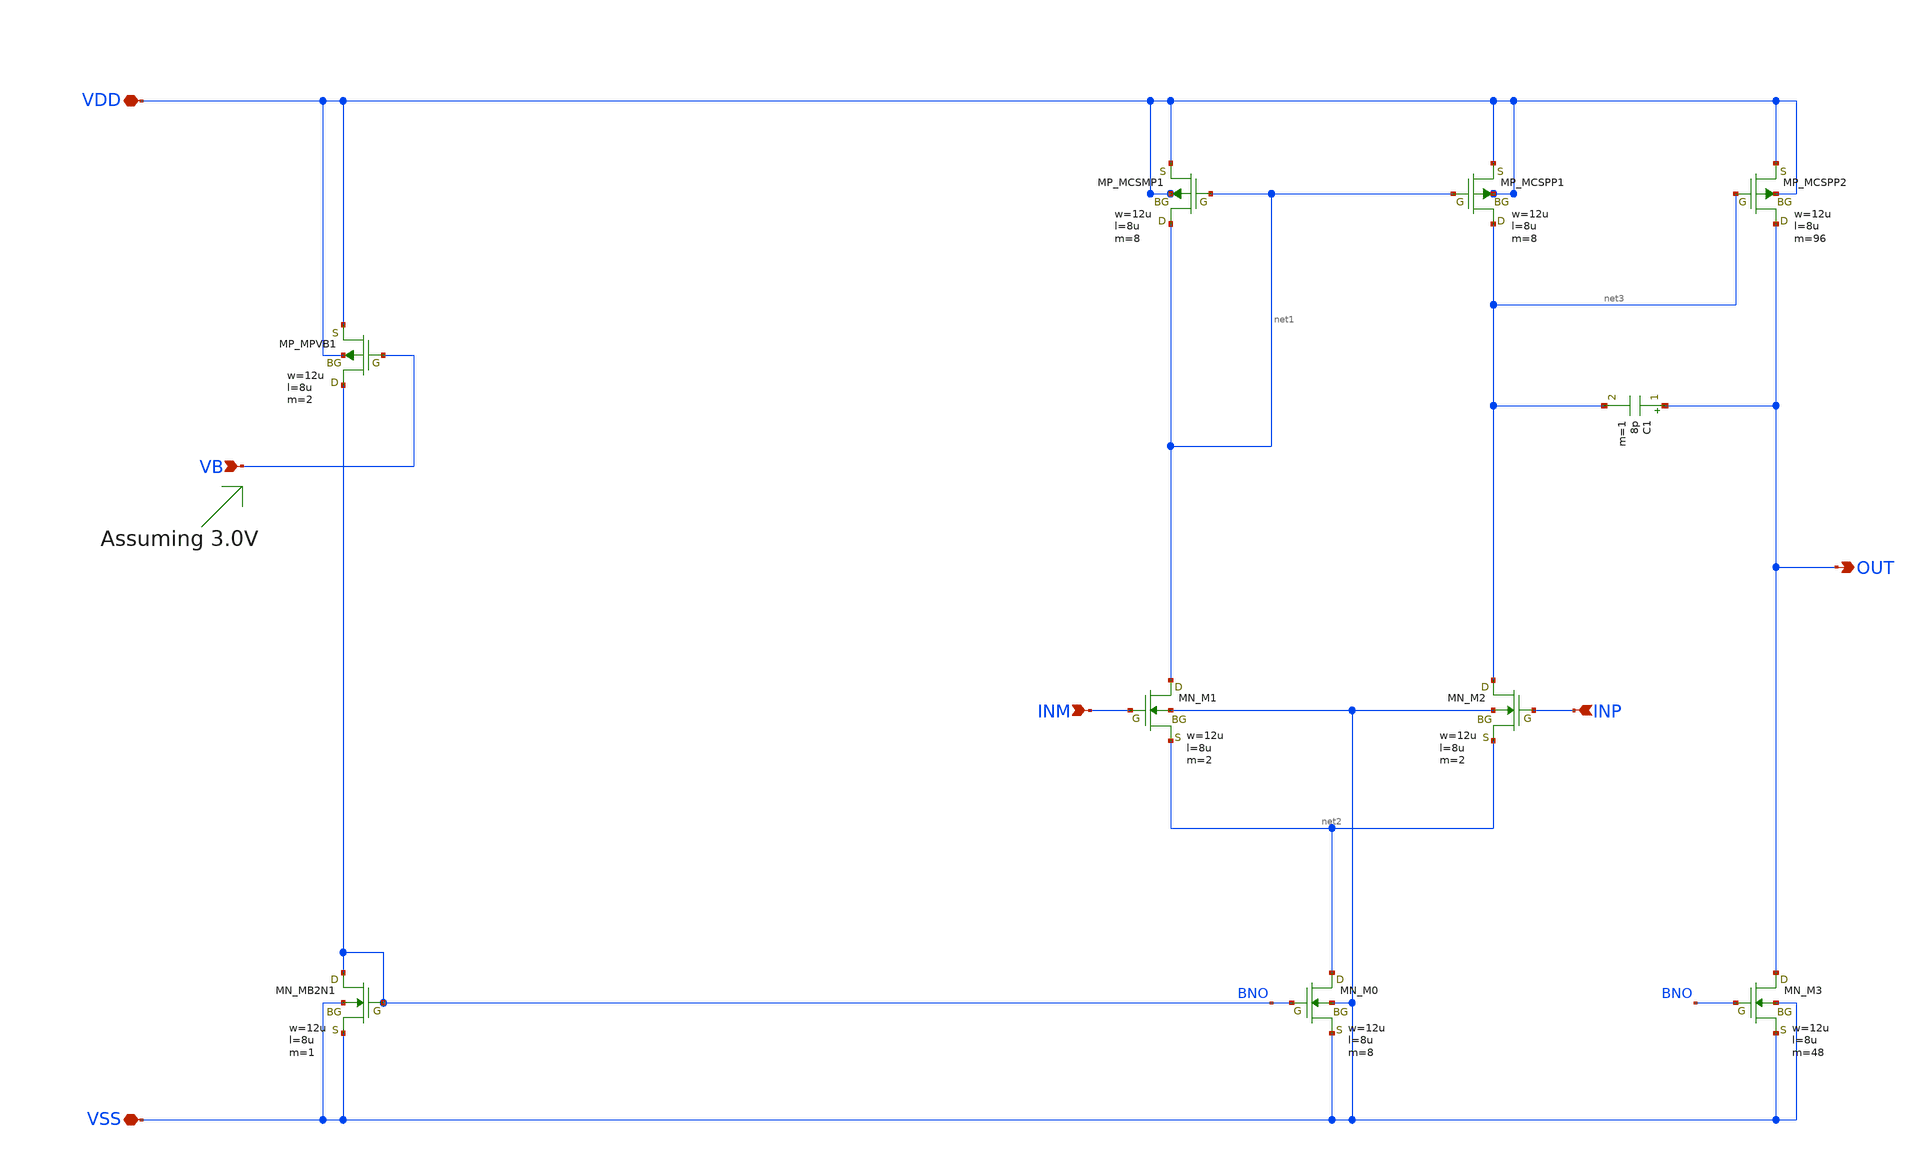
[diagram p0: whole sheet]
** sch_path: OpenSUSI-TR10/opamp_r2r/ota_noccm_sf.sch
**.subckt ota_noccm_sf VDD VSS INM INP VB OUT
*.iopin VDD
*.iopin VSS
*.ipin INM
*.ipin INP
*.ipin VB
*.opin OUT
XMB2N1 BNO BNO VSS VSS NMOS w=12u l=8u as=0 ad=0 ps=0 pd=0 nrd=0 nrs=0 m=1
XM0 net2 BNO VSS VSS NMOS w=12u l=8u as=0 ad=0 ps=0 pd=0 nrd=0 nrs=0 m=8
XM1 net1 INM net2 VSS NMOS w=12u l=8u as=0 ad=0 ps=0 pd=0 nrd=0 nrs=0 m=2
XM2 net3 INP net2 VSS NMOS w=12u l=8u as=0 ad=0 ps=0 pd=0 nrd=0 nrs=0 m=2
XMCSMP1 net1 net1 VDD VDD PMOS w=12u l=8u as=0 ad=0 ps=0 pd=0 nrd=0 nrs=0 m=8
XMCSPP1 net3 net1 VDD VDD PMOS w=12u l=8u as=0 ad=0 ps=0 pd=0 nrd=0 nrs=0 m=8
XMPVB1 BNO VB VDD VDD PMOS w=12u l=8u as=0 ad=0 ps=0 pd=0 nrd=0 nrs=0 m=2
XM3 OUT BNO VSS VSS NMOS w=12u l=8u as=0 ad=0 ps=0 pd=0 nrd=0 nrs=0 m=48
XMCSPP2 OUT net3 VDD VDD PMOS w=12u l=8u as=0 ad=0 ps=0 pd=0 nrd=0 nrs=0 m=96
C1 OUT net3 8p m=1
**.ends
.end
